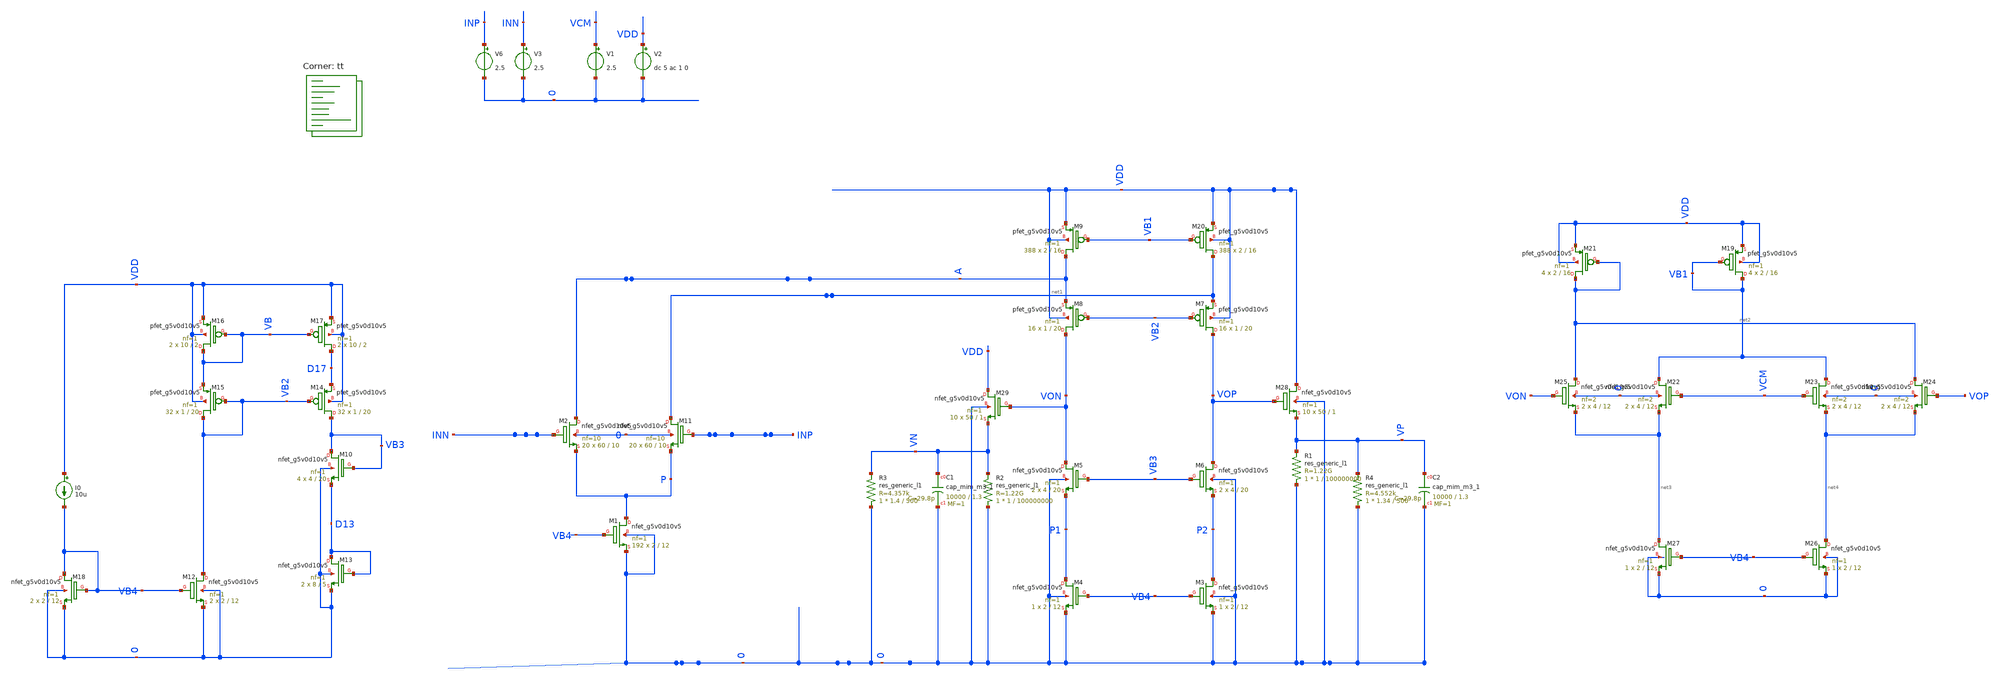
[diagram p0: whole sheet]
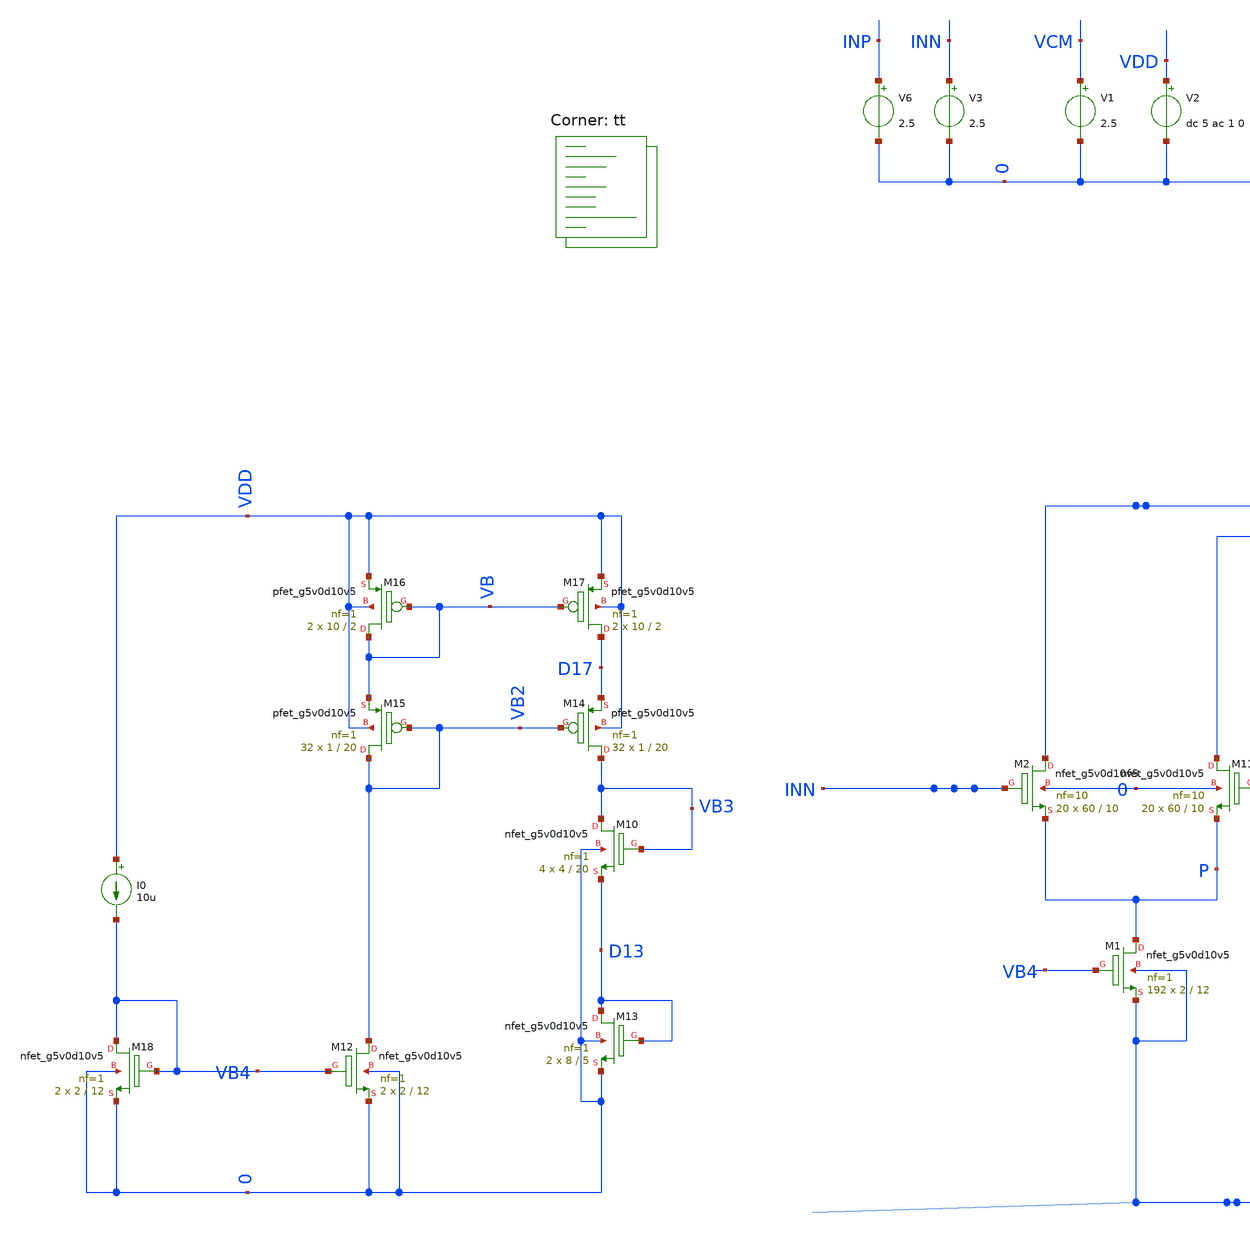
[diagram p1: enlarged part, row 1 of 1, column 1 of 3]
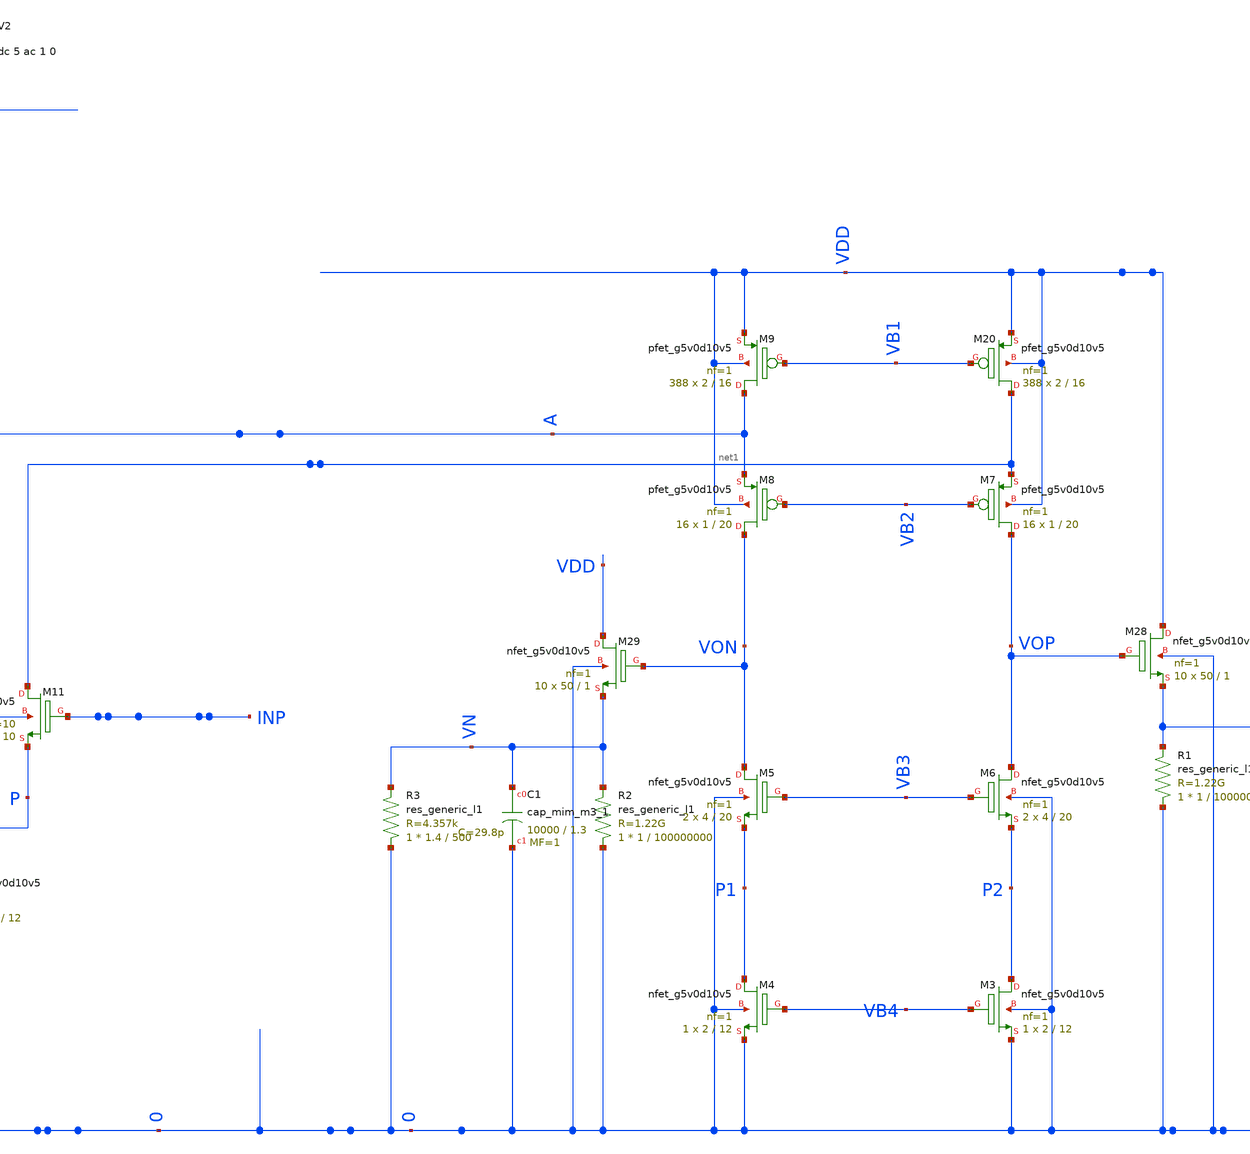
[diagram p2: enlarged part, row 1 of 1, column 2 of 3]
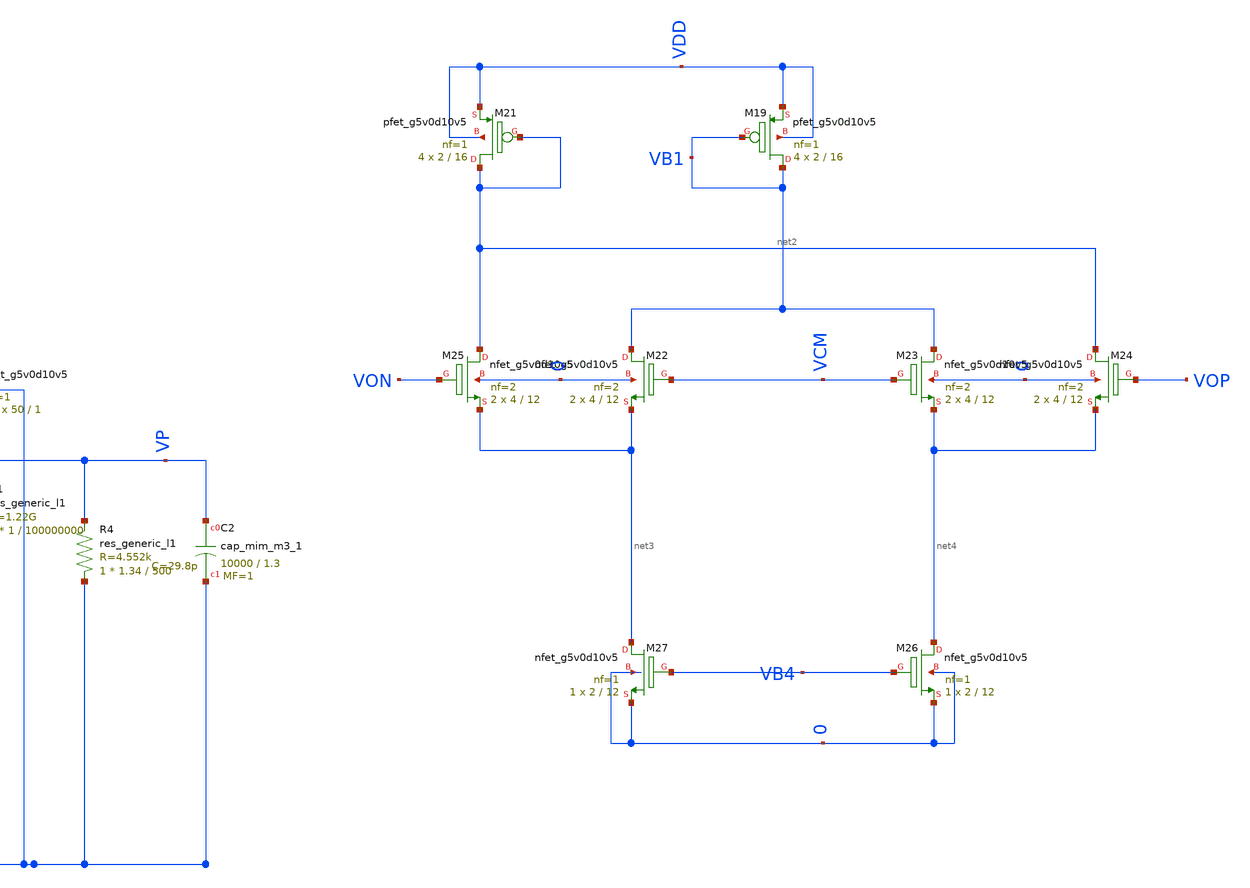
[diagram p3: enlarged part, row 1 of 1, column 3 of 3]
** sch_path: High_Gain_Operation_Amplifier/Folded_trans.sch
**.subckt Folded_trans
I0 VDD VB4 10u
V6 INP 0 2.5
XM13 D13 D13 0 0 sky130_fd_pr__nfet_g5v0d10v5 L=5 W=8 nf=1 ad='int((nf+1)/2) * W/nf * 0.29' as='int((nf+2)/2) * W/nf * 0.29'
+ pd='2*int((nf+1)/2) * (W/nf + 0.29)' ps='2*int((nf+2)/2) * (W/nf + 0.29)' nrd='0.29 / W' nrs='0.29 / W'
+ sa=0 sb=0 sd=0 mult=2 m=2
XM12 VB2 VB4 0 0 sky130_fd_pr__nfet_g5v0d10v5 L=12 W=2 nf=1 ad='int((nf+1)/2) * W/nf * 0.29' as='int((nf+2)/2) * W/nf * 0.29'
+ pd='2*int((nf+1)/2) * (W/nf + 0.29)' ps='2*int((nf+2)/2) * (W/nf + 0.29)' nrd='0.29 / W' nrs='0.29 / W'
+ sa=0 sb=0 sd=0 mult=2 m=2
XM18 VB4 VB4 0 0 sky130_fd_pr__nfet_g5v0d10v5 L=12 W=2 nf=1 ad='int((nf+1)/2) * W/nf * 0.29' as='int((nf+2)/2) * W/nf * 0.29'
+ pd='2*int((nf+1)/2) * (W/nf + 0.29)' ps='2*int((nf+2)/2) * (W/nf + 0.29)' nrd='0.29 / W' nrs='0.29 / W'
+ sa=0 sb=0 sd=0 mult=2 m=2
XM15 VB2 VB2 VB VDD sky130_fd_pr__pfet_g5v0d10v5 L=20 W=1 nf=1 ad='int((nf+1)/2) * W/nf * 0.29' as='int((nf+2)/2) * W/nf * 0.29'
+ pd='2*int((nf+1)/2) * (W/nf + 0.29)' ps='2*int((nf+2)/2) * (W/nf + 0.29)' nrd='0.29 / W' nrs='0.29 / W'
+ sa=0 sb=0 sd=0 mult=32 m=32
XM16 VB VB VDD VDD sky130_fd_pr__pfet_g5v0d10v5 L=2 W=10 nf=1 ad='int((nf+1)/2) * W/nf * 0.29' as='int((nf+2)/2) * W/nf * 0.29'
+ pd='2*int((nf+1)/2) * (W/nf + 0.29)' ps='2*int((nf+2)/2) * (W/nf + 0.29)' nrd='0.29 / W' nrs='0.29 / W'
+ sa=0 sb=0 sd=0 mult=2 m=2
XM17 D17 VB VDD VDD sky130_fd_pr__pfet_g5v0d10v5 L=2 W=10 nf=1 ad='int((nf+1)/2) * W/nf * 0.29' as='int((nf+2)/2) * W/nf * 0.29'
+ pd='2*int((nf+1)/2) * (W/nf + 0.29)' ps='2*int((nf+2)/2) * (W/nf + 0.29)' nrd='0.29 / W' nrs='0.29 / W'
+ sa=0 sb=0 sd=0 mult=2 m=2
XM14 VB3 VB2 D17 VDD sky130_fd_pr__pfet_g5v0d10v5 L=20 W=1 nf=1 ad='int((nf+1)/2) * W/nf * 0.29' as='int((nf+2)/2) * W/nf * 0.29'
+ pd='2*int((nf+1)/2) * (W/nf + 0.29)' ps='2*int((nf+2)/2) * (W/nf + 0.29)' nrd='0.29 / W' nrs='0.29 / W'
+ sa=0 sb=0 sd=0 mult=32 m=32
XM1 P VB4 0 0 sky130_fd_pr__nfet_g5v0d10v5 L=12 W=2 nf=1 ad='int((nf+1)/2) * W/nf * 0.29' as='int((nf+2)/2) * W/nf * 0.29'
+ pd='2*int((nf+1)/2) * (W/nf + 0.29)' ps='2*int((nf+2)/2) * (W/nf + 0.29)' nrd='0.29 / W' nrs='0.29 / W'
+ sa=0 sb=0 sd=0 mult=192 m=192
XM2 A INN P 0 sky130_fd_pr__nfet_g5v0d10v5 L=10 W=60 nf=10 ad='int((nf+1)/2) * W/nf * 0.29' as='int((nf+2)/2) * W/nf * 0.29'
+ pd='2*int((nf+1)/2) * (W/nf + 0.29)' ps='2*int((nf+2)/2) * (W/nf + 0.29)' nrd='0.29 / W' nrs='0.29 / W'
+ sa=0 sb=0 sd=0 mult=20 m=20
XM11 net1 INP P 0 sky130_fd_pr__nfet_g5v0d10v5 L=10 W=60 nf=10 ad='int((nf+1)/2) * W/nf * 0.29' as='int((nf+2)/2) * W/nf * 0.29'
+ pd='2*int((nf+1)/2) * (W/nf + 0.29)' ps='2*int((nf+2)/2) * (W/nf + 0.29)' nrd='0.29 / W' nrs='0.29 / W'
+ sa=0 sb=0 sd=0 mult=20 m=20
XM20 net1 VB1 VDD VDD sky130_fd_pr__pfet_g5v0d10v5 L=16 W=2 nf=1 ad='int((nf+1)/2) * W/nf * 0.29' as='int((nf+2)/2) * W/nf * 0.29'
+ pd='2*int((nf+1)/2) * (W/nf + 0.29)' ps='2*int((nf+2)/2) * (W/nf + 0.29)' nrd='0.29 / W' nrs='0.29 / W'
+ sa=0 sb=0 sd=0 mult=388 m=388
XM9 A VB1 VDD VDD sky130_fd_pr__pfet_g5v0d10v5 L=16 W=2 nf=1 ad='int((nf+1)/2) * W/nf * 0.29' as='int((nf+2)/2) * W/nf * 0.29'
+ pd='2*int((nf+1)/2) * (W/nf + 0.29)' ps='2*int((nf+2)/2) * (W/nf + 0.29)' nrd='0.29 / W' nrs='0.29 / W'
+ sa=0 sb=0 sd=0 mult=388 m=388
XM7 VOP VB2 net1 VDD sky130_fd_pr__pfet_g5v0d10v5 L=20 W=1 nf=1 ad='int((nf+1)/2) * W/nf * 0.29' as='int((nf+2)/2) * W/nf * 0.29'
+ pd='2*int((nf+1)/2) * (W/nf + 0.29)' ps='2*int((nf+2)/2) * (W/nf + 0.29)' nrd='0.29 / W' nrs='0.29 / W'
+ sa=0 sb=0 sd=0 mult=16 m=16
XM8 VON VB2 A VDD sky130_fd_pr__pfet_g5v0d10v5 L=20 W=1 nf=1 ad='int((nf+1)/2) * W/nf * 0.29' as='int((nf+2)/2) * W/nf * 0.29'
+ pd='2*int((nf+1)/2) * (W/nf + 0.29)' ps='2*int((nf+2)/2) * (W/nf + 0.29)' nrd='0.29 / W' nrs='0.29 / W'
+ sa=0 sb=0 sd=0 mult=16 m=16
XM3 P2 VB4 0 0 sky130_fd_pr__nfet_g5v0d10v5 L=12 W=2 nf=1 ad='int((nf+1)/2) * W/nf * 0.29' as='int((nf+2)/2) * W/nf * 0.29'
+ pd='2*int((nf+1)/2) * (W/nf + 0.29)' ps='2*int((nf+2)/2) * (W/nf + 0.29)' nrd='0.29 / W' nrs='0.29 / W'
+ sa=0 sb=0 sd=0 mult=1 m=1
XM4 P1 VB4 0 0 sky130_fd_pr__nfet_g5v0d10v5 L=12 W=2 nf=1 ad='int((nf+1)/2) * W/nf * 0.29' as='int((nf+2)/2) * W/nf * 0.29'
+ pd='2*int((nf+1)/2) * (W/nf + 0.29)' ps='2*int((nf+2)/2) * (W/nf + 0.29)' nrd='0.29 / W' nrs='0.29 / W'
+ sa=0 sb=0 sd=0 mult=1 m=1
XM5 VON VB3 P1 0 sky130_fd_pr__nfet_g5v0d10v5 L=20 W=4 nf=1 ad='int((nf+1)/2) * W/nf * 0.29' as='int((nf+2)/2) * W/nf * 0.29'
+ pd='2*int((nf+1)/2) * (W/nf + 0.29)' ps='2*int((nf+2)/2) * (W/nf + 0.29)' nrd='0.29 / W' nrs='0.29 / W'
+ sa=0 sb=0 sd=0 mult=2 m=2
XM6 VOP VB3 P2 0 sky130_fd_pr__nfet_g5v0d10v5 L=20 W=4 nf=1 ad='int((nf+1)/2) * W/nf * 0.29' as='int((nf+2)/2) * W/nf * 0.29'
+ pd='2*int((nf+1)/2) * (W/nf + 0.29)' ps='2*int((nf+2)/2) * (W/nf + 0.29)' nrd='0.29 / W' nrs='0.29 / W'
+ sa=0 sb=0 sd=0 mult=2 m=2
XM10 VB3 VB3 D13 0 sky130_fd_pr__nfet_g5v0d10v5 L=20 W=4 nf=1 ad='int((nf+1)/2) * W/nf * 0.29' as='int((nf+2)/2) * W/nf * 0.29'
+ pd='2*int((nf+1)/2) * (W/nf + 0.29)' ps='2*int((nf+2)/2) * (W/nf + 0.29)' nrd='0.29 / W' nrs='0.29 / W'
+ sa=0 sb=0 sd=0 mult=4 m=4
XM19 VB1 VB1 VDD VDD sky130_fd_pr__pfet_g5v0d10v5 L=16 W=2 nf=1 ad='int((nf+1)/2) * W/nf * 0.29' as='int((nf+2)/2) * W/nf * 0.29'
+ pd='2*int((nf+1)/2) * (W/nf + 0.29)' ps='2*int((nf+2)/2) * (W/nf + 0.29)' nrd='0.29 / W' nrs='0.29 / W'
+ sa=0 sb=0 sd=0 mult=4 m=4
XM21 net2 net2 VDD VDD sky130_fd_pr__pfet_g5v0d10v5 L=16 W=2 nf=1 ad='int((nf+1)/2) * W/nf * 0.29' as='int((nf+2)/2) * W/nf * 0.29'
+ pd='2*int((nf+1)/2) * (W/nf + 0.29)' ps='2*int((nf+2)/2) * (W/nf + 0.29)' nrd='0.29 / W' nrs='0.29 / W'
+ sa=0 sb=0 sd=0 mult=4 m=4
XM22 VB1 VCM net3 0 sky130_fd_pr__nfet_g5v0d10v5 L=12 W=4 nf=2 ad='int((nf+1)/2) * W/nf * 0.29' as='int((nf+2)/2) * W/nf * 0.29'
+ pd='2*int((nf+1)/2) * (W/nf + 0.29)' ps='2*int((nf+2)/2) * (W/nf + 0.29)' nrd='0.29 / W' nrs='0.29 / W'
+ sa=0 sb=0 sd=0 mult=2 m=2
XM24 net2 VOP net4 0 sky130_fd_pr__nfet_g5v0d10v5 L=12 W=4 nf=2 ad='int((nf+1)/2) * W/nf * 0.29' as='int((nf+2)/2) * W/nf * 0.29'
+ pd='2*int((nf+1)/2) * (W/nf + 0.29)' ps='2*int((nf+2)/2) * (W/nf + 0.29)' nrd='0.29 / W' nrs='0.29 / W'
+ sa=0 sb=0 sd=0 mult=2 m=2
XM25 net2 VON net3 0 sky130_fd_pr__nfet_g5v0d10v5 L=12 W=4 nf=2 ad='int((nf+1)/2) * W/nf * 0.29' as='int((nf+2)/2) * W/nf * 0.29'
+ pd='2*int((nf+1)/2) * (W/nf + 0.29)' ps='2*int((nf+2)/2) * (W/nf + 0.29)' nrd='0.29 / W' nrs='0.29 / W'
+ sa=0 sb=0 sd=0 mult=2 m=2
XM26 net4 VB4 0 0 sky130_fd_pr__nfet_g5v0d10v5 L=12 W=2 nf=1 ad='int((nf+1)/2) * W/nf * 0.29' as='int((nf+2)/2) * W/nf * 0.29'
+ pd='2*int((nf+1)/2) * (W/nf + 0.29)' ps='2*int((nf+2)/2) * (W/nf + 0.29)' nrd='0.29 / W' nrs='0.29 / W'
+ sa=0 sb=0 sd=0 mult=1 m=1
XM27 net3 VB4 0 0 sky130_fd_pr__nfet_g5v0d10v5 L=12 W=2 nf=1 ad='int((nf+1)/2) * W/nf * 0.29' as='int((nf+2)/2) * W/nf * 0.29'
+ pd='2*int((nf+1)/2) * (W/nf + 0.29)' ps='2*int((nf+2)/2) * (W/nf + 0.29)' nrd='0.29 / W' nrs='0.29 / W'
+ sa=0 sb=0 sd=0 mult=1 m=1
V1 VCM 0 2.5
XM23 VB1 VCM net4 0 sky130_fd_pr__nfet_g5v0d10v5 L=12 W=4 nf=2 ad='int((nf+1)/2) * W/nf * 0.29' as='int((nf+2)/2) * W/nf * 0.29'
+ pd='2*int((nf+1)/2) * (W/nf + 0.29)' ps='2*int((nf+2)/2) * (W/nf + 0.29)' nrd='0.29 / W' nrs='0.29 / W'
+ sa=0 sb=0 sd=0 mult=2 m=2
XM28 VDD VOP VP 0 sky130_fd_pr__nfet_g5v0d10v5 L=1 W=50 nf=1 ad='int((nf+1)/2) * W/nf * 0.29' as='int((nf+2)/2) * W/nf * 0.29'
+ pd='2*int((nf+1)/2) * (W/nf + 0.29)' ps='2*int((nf+2)/2) * (W/nf + 0.29)' nrd='0.29 / W' nrs='0.29 / W'
+ sa=0 sb=0 sd=0 mult=10 m=10
R1 0 VP sky130_fd_pr__res_generic_l1 W=1 L=100000000 m=1
XM29 VDD VON VN 0 sky130_fd_pr__nfet_g5v0d10v5 L=1 W=50 nf=1 ad='int((nf+1)/2) * W/nf * 0.29' as='int((nf+2)/2) * W/nf * 0.29'
+ pd='2*int((nf+1)/2) * (W/nf + 0.29)' ps='2*int((nf+2)/2) * (W/nf + 0.29)' nrd='0.29 / W' nrs='0.29 / W'
+ sa=0 sb=0 sd=0 mult=10 m=10
R2 0 VN sky130_fd_pr__res_generic_l1 W=1 L=100000000 m=1
XC1 VN 0 sky130_fd_pr__cap_mim_m3_1 W=10000 L=1.3 MF=1 m=1
R3 0 VN sky130_fd_pr__res_generic_l1 W=1.4 L=500 m=1
XC2 VP 0 sky130_fd_pr__cap_mim_m3_1 W=10000 L=1.3 MF=1 m=1
R4 0 VP sky130_fd_pr__res_generic_l1 W=1.34 L=500 m=1
V2 VDD 0 dc 5 ac 1 0
V3 INN 0 2.5
**** begin user architecture code

* this option enables mos model bin
* selection based on W/NF instead of W
.option wnflag=1
.option savecurrents

.control
save all
save @m.xm15.msky130_fd_pr__pfet_g5v0d10v5[vth]
save @m.xm15.msky130_fd_pr__pfet_g5v0d10v5[gm]
save @m.xm9.msky130_fd_pr__pfet_g5v0d10v5[vth]
save @m.xm9.msky130_fd_pr__pfet_g5v0d10v5[gm]
save @m.xm8.msky130_fd_pr__pfet_g5v0d10v5[vth]
save @m.xm8.msky130_fd_pr__pfet_g5v0d10v5[gm]
save @m.xm20.msky130_fd_pr__pfet_g5v0d10v5[vth]
save @m.xm20.msky130_fd_pr__pfet_g5v0d10v5[gm]
save @m.xm7.msky130_fd_pr__pfet_g5v0d10v5[vth]
save @m.xm7.msky130_fd_pr__pfet_g5v0d10v5[gm]
save @m.xm10.msky130_fd_pr__nfet_g5v0d10v5[gm]
save @m.xm10.msky130_fd_pr__nfet_g5v0d10v5[vth]
save @m.xm14.msky130_fd_pr__pfet_g5v0d10v5[gm]
save @m.xm14.msky130_fd_pr__pfet_g5v0d10v5[vth]
save @m.xm16.msky130_fd_pr__pfet_g5v0d10v5[gm]
save @m.xm16.msky130_fd_pr__pfet_g5v0d10v5[vth]
save @m.xm17.msky130_fd_pr__pfet_g5v0d10v5[gm]
save @m.xm17.msky130_fd_pr__pfet_g5v0d10v5[vth]
save @m.xm13.msky130_fd_pr__nfet_g5v0d10v5[gm]
save @m.xm13.msky130_fd_pr__nfet_g5v0d10v5[vth]
save @m.xm12.msky130_fd_pr__nfet_g5v0d10v5[vth]
save @m.xm18.msky130_fd_pr__nfet_g5v0d10v5[vth]
*folded
save @m.xm2.msky130_fd_pr__nfet_g5v0d10v5[vth]
save @m.xm11.msky130_fd_pr__nfet_g5v0d10v5[vth]
save @m.xm1.msky130_fd_pr__nfet_g5v0d10v5[vth]
save @m.xm5.msky130_fd_pr__nfet_g5v0d10v5[vth]
save @m.xm6.msky130_fd_pr__nfet_g5v0d10v5[vth]
save @m.xm4.msky130_fd_pr__nfet_g5v0d10v5[vth]
save @m.xm3.msky130_fd_pr__nfet_g5v0d10v5[vth]
save @m.xm7.msky130_fd_pr__pfet_g5v0d10v5[vth]
save @m.xm8.msky130_fd_pr__pfet_g5v0d10v5[vth]
save @m.xm9.msky130_fd_pr__pfet_g5v0d10v5[vth]
save @m.xm20.msky130_fd_pr__pfet_g5v0d10v5[vth]
*CMFB
save @m.xm21.msky130_fd_pr__pfet_g5v0d10v5[vth]
save @m.xm19.msky130_fd_pr__pfet_g5v0d10v5[vth]
save @m.xm22.msky130_fd_pr__nfet_g5v0d10v5[vth]
save @m.xm23.msky130_fd_pr__nfet_g5v0d10v5[vth]
save @m.xm25.msky130_fd_pr__nfet_g5v0d10v5[vth]
save @m.xm27.msky130_fd_pr__nfet_g5v0d10v5[vth]
save @m.xm26.msky130_fd_pr__nfet_g5v0d10v5[vth]
save @m.xm24.msky130_fd_pr__nfet_g5v0d10v5[vth]
save current


write Folded_trans.raw
trans 10u 1u 1m
op
print VON VOP VB2 VB
*print @m.xm18.msky130_fd_pr__nfet_g5v0d10v5
*print @m.xm12.msky130_fd_pr__nfet_g5v0d10v5
*print @m.xm13.msky130_fd_pr__nfet_g5v0d10v5
*print @m.xm10.msky130_fd_pr__nfet_g5v0d10v5
*print @m.xm14.msky130_fd_pr__pfet_g5v0d10v5
*print @m.xm17.msky130_fd_pr__pfet_g5v0d10v5
*print @m.xm15.msky130_fd_pr__pfet_g5v0d10v5
*print @m.xm16.msky130_fd_pr__pfet_g5v0d10v5
*Folded cascode
*print @m.xm9.msky130_fd_pr__pfet_g5v0d10v5
*print @m.xm8.msky130_fd_pr__pfet_g5v0d10v5
*print @m.xm5.msky130_fd_pr__nfet_g5v0d10v5
*print @m.xm4.msky130_fd_pr__nfet_g5v0d10v5
*print @m.xm1.msky130_fd_pr__nfet_g5v0d10v5
*print @m.xm2.msky130_fd_pr__nfet_g5v0d10v5
*print @m.xm11.msky130_fd_pr__nfet_g5v0d10v5
*CMFB
*print @m.xm23.msky130_fd_pr__nfet_g5v0d10v5
*print @m.xm24.msky130_fd_pr__nfet_g5v0d10v5
*print @m.xm25.msky130_fd_pr__nfet_g5v0d10v5
*print @m.xm22.msky130_fd_pr__nfet_g5v0d10v5
print @m.xm9.msky130_fd_pr__pfet_g5v0d10v5
print @m.xm8.msky130_fd_pr__pfet_g5v0d10v5
print @m.xm4.msky130_fd_pr__nfet_g5v0d10v5
print @m.xm5.msky130_fd_pr__nfet_g5v0d10v5
write Folded_trans.raw
ac dec 10 1 1e9
  remzerovec
  write Folded_trans.raw
quit 0
.endc


.lib $::SKYWATER_MODELS/sky130.lib.spice tt
**** end user architecture code
**.ends
.end
